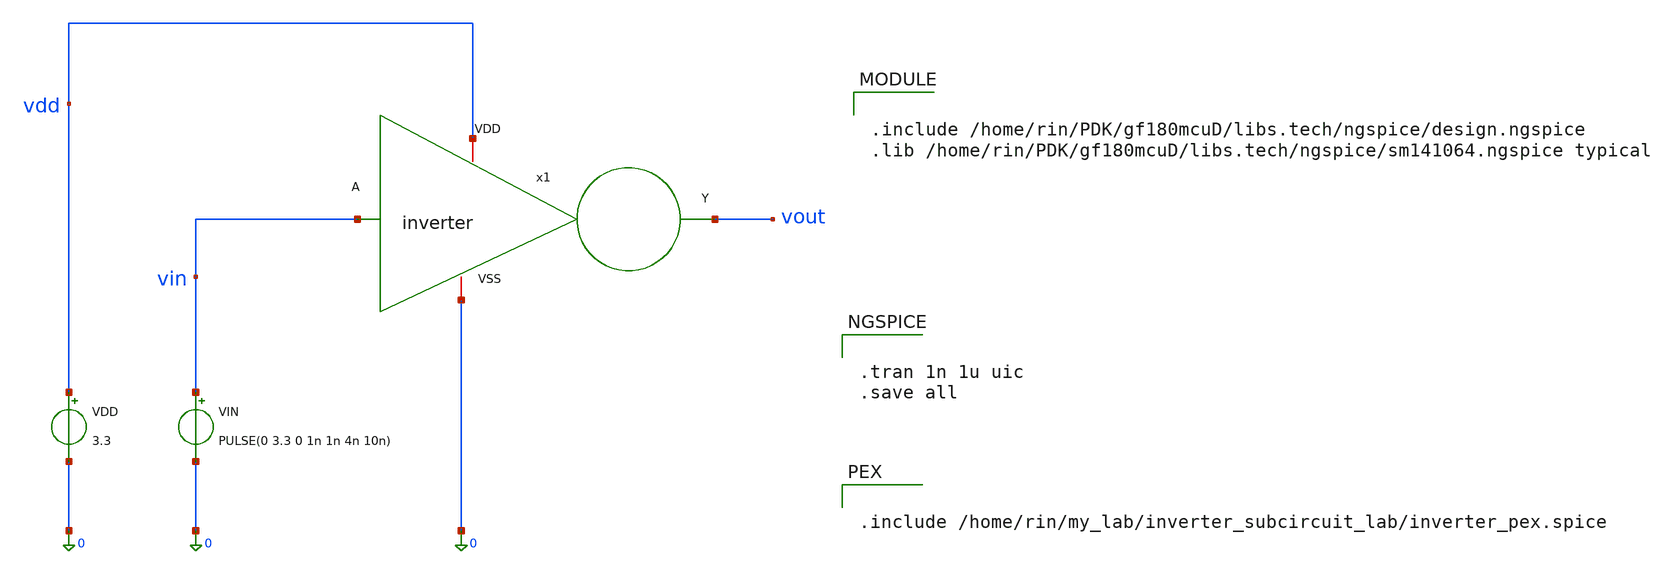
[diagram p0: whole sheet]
** sch_path: inverter_subcircuit.sch
**.subckt inverter_subcircuit
x1 vdd vin vout 0 inverter
VDD vdd 0 3.3
VIN vin 0 PULSE(0 3.3 0 1n 1n 4n 10n)
**** begin user architecture code


.include /home/rin/PDK/gf180mcuD/libs.tech/ngspice/design.ngspice
.lib /home/rin/PDK/gf180mcuD/libs.tech/ngspice/sm141064.ngspice typical




.tran 1n 1u uic
.save all




.include /home/rin/my_lab/inverter_subcircuit_lab/inverter_pex.spice


**** end user architecture code
**.ends
.end
